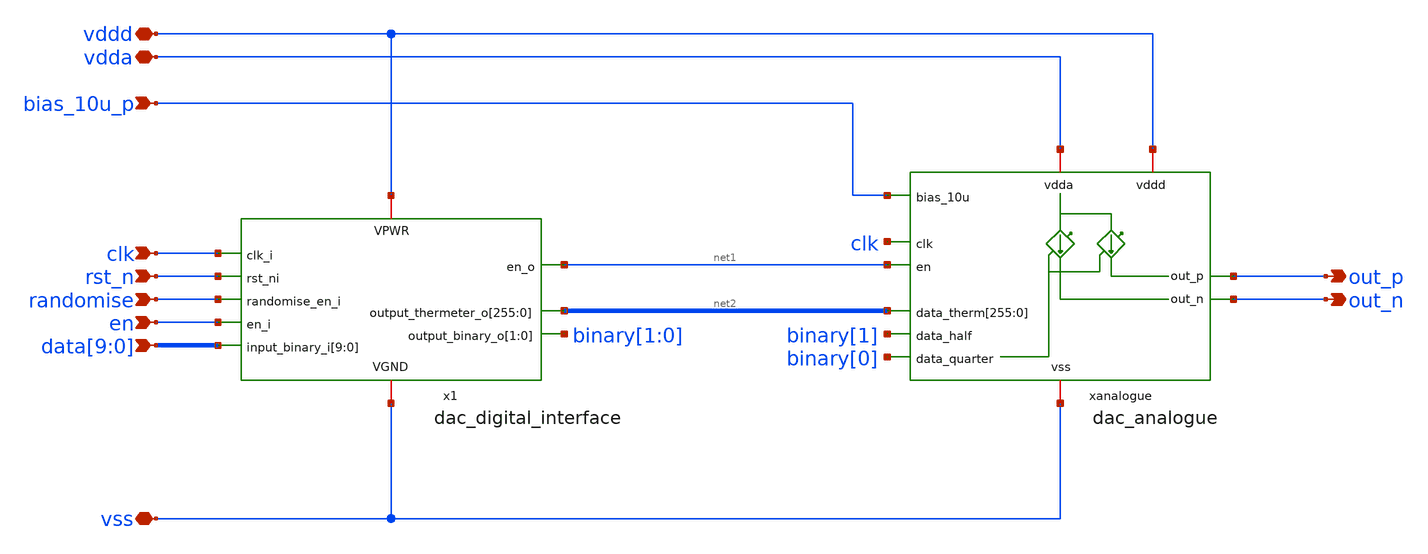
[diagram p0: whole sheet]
** sch_path: design/dac/dac.sch
**.subckt dac vss vdda vddd bias_10u_p clk
*+ data[9],data[8],data[7],data[6],data[5],data[4],data[3],data[2],data[1],data[0] out_p out_n en randomise rst_n
*.iopin vss
*.iopin vdda
*.iopin vddd
*.ipin bias_10u_p
*.ipin clk
*.ipin data[9],data[8],data[7],data[6],data[5],data[4],data[3],data[2],data[1],data[0]
*.opin out_p
*.opin out_n
*.ipin en
*.ipin randomise
*.ipin rst_n
xanalogue vdda vddd bias_10u_p clk net1 net2[255] net2[254] net2[253] net2[252] net2[251] net2[250]
+ net2[249] net2[248] net2[247] net2[246] net2[245] net2[244] net2[243] net2[242] net2[241] net2[240] net2[239]
+ net2[238] net2[237] net2[236] net2[235] net2[234] net2[233] net2[232] net2[231] net2[230] net2[229] net2[228]
+ net2[227] net2[226] net2[225] net2[224] net2[223] net2[222] net2[221] net2[220] net2[219] net2[218] net2[217]
+ net2[216] net2[215] net2[214] net2[213] net2[212] net2[211] net2[210] net2[209] net2[208] net2[207] net2[206]
+ net2[205] net2[204] net2[203] net2[202] net2[201] net2[200] net2[199] net2[198] net2[197] net2[196] net2[195]
+ net2[194] net2[193] net2[192] net2[191] net2[190] net2[189] net2[188] net2[187] net2[186] net2[185] net2[184]
+ net2[183] net2[182] net2[181] net2[180] net2[179] net2[178] net2[177] net2[176] net2[175] net2[174] net2[173]
+ net2[172] net2[171] net2[170] net2[169] net2[168] net2[167] net2[166] net2[165] net2[164] net2[163] net2[162]
+ net2[161] net2[160] net2[159] net2[158] net2[157] net2[156] net2[155] net2[154] net2[153] net2[152] net2[151]
+ net2[150] net2[149] net2[148] net2[147] net2[146] net2[145] net2[144] net2[143] net2[142] net2[141] net2[140]
+ net2[139] net2[138] net2[137] net2[136] net2[135] net2[134] net2[133] net2[132] net2[131] net2[130] net2[129]
+ net2[128] net2[127] net2[126] net2[125] net2[124] net2[123] net2[122] net2[121] net2[120] net2[119] net2[118]
+ net2[117] net2[116] net2[115] net2[114] net2[113] net2[112] net2[111] net2[110] net2[109] net2[108] net2[107]
+ net2[106] net2[105] net2[104] net2[103] net2[102] net2[101] net2[100] net2[99] net2[98] net2[97] net2[96]
+ net2[95] net2[94] net2[93] net2[92] net2[91] net2[90] net2[89] net2[88] net2[87] net2[86] net2[85] net2[84]
+ net2[83] net2[82] net2[81] net2[80] net2[79] net2[78] net2[77] net2[76] net2[75] net2[74] net2[73] net2[72]
+ net2[71] net2[70] net2[69] net2[68] net2[67] net2[66] net2[65] net2[64] net2[63] net2[62] net2[61] net2[60]
+ net2[59] net2[58] net2[57] net2[56] net2[55] net2[54] net2[53] net2[52] net2[51] net2[50] net2[49] net2[48]
+ net2[47] net2[46] net2[45] net2[44] net2[43] net2[42] net2[41] net2[40] net2[39] net2[38] net2[37] net2[36]
+ net2[35] net2[34] net2[33] net2[32] net2[31] net2[30] net2[29] net2[28] net2[27] net2[26] net2[25] net2[24]
+ net2[23] net2[22] net2[21] net2[20] net2[19] net2[18] net2[17] net2[16] net2[15] net2[14] net2[13] net2[12]
+ net2[11] net2[10] net2[9] net2[8] net2[7] net2[6] net2[5] net2[4] net2[3] net2[2] net2[1] net2[0] binary[1]
+ binary[0] out_p out_n vss dac_analogue
x1 vddd clk net2[255] net2[254] net2[253] net2[252] net2[251] net2[250] net2[249] net2[248]
+ net2[247] net2[246] net2[245] net2[244] net2[243] net2[242] net2[241] net2[240] net2[239] net2[238] net2[237]
+ net2[236] net2[235] net2[234] net2[233] net2[232] net2[231] net2[230] net2[229] net2[228] net2[227] net2[226]
+ net2[225] net2[224] net2[223] net2[222] net2[221] net2[220] net2[219] net2[218] net2[217] net2[216] net2[215]
+ net2[214] net2[213] net2[212] net2[211] net2[210] net2[209] net2[208] net2[207] net2[206] net2[205] net2[204]
+ net2[203] net2[202] net2[201] net2[200] net2[199] net2[198] net2[197] net2[196] net2[195] net2[194] net2[193]
+ net2[192] net2[191] net2[190] net2[189] net2[188] net2[187] net2[186] net2[185] net2[184] net2[183] net2[182]
+ net2[181] net2[180] net2[179] net2[178] net2[177] net2[176] net2[175] net2[174] net2[173] net2[172] net2[171]
+ net2[170] net2[169] net2[168] net2[167] net2[166] net2[165] net2[164] net2[163] net2[162] net2[161] net2[160]
+ net2[159] net2[158] net2[157] net2[156] net2[155] net2[154] net2[153] net2[152] net2[151] net2[150] net2[149]
+ net2[148] net2[147] net2[146] net2[145] net2[144] net2[143] net2[142] net2[141] net2[140] net2[139] net2[138]
+ net2[137] net2[136] net2[135] net2[134] net2[133] net2[132] net2[131] net2[130] net2[129] net2[128] net2[127]
+ net2[126] net2[125] net2[124] net2[123] net2[122] net2[121] net2[120] net2[119] net2[118] net2[117] net2[116]
+ net2[115] net2[114] net2[113] net2[112] net2[111] net2[110] net2[109] net2[108] net2[107] net2[106] net2[105]
+ net2[104] net2[103] net2[102] net2[101] net2[100] net2[99] net2[98] net2[97] net2[96] net2[95] net2[94]
+ net2[93] net2[92] net2[91] net2[90] net2[89] net2[88] net2[87] net2[86] net2[85] net2[84] net2[83] net2[82]
+ net2[81] net2[80] net2[79] net2[78] net2[77] net2[76] net2[75] net2[74] net2[73] net2[72] net2[71] net2[70]
+ net2[69] net2[68] net2[67] net2[66] net2[65] net2[64] net2[63] net2[62] net2[61] net2[60] net2[59] net2[58]
+ net2[57] net2[56] net2[55] net2[54] net2[53] net2[52] net2[51] net2[50] net2[49] net2[48] net2[47] net2[46]
+ net2[45] net2[44] net2[43] net2[42] net2[41] net2[40] net2[39] net2[38] net2[37] net2[36] net2[35] net2[34]
+ net2[33] net2[32] net2[31] net2[30] net2[29] net2[28] net2[27] net2[26] net2[25] net2[24] net2[23] net2[22]
+ net2[21] net2[20] net2[19] net2[18] net2[17] net2[16] net2[15] net2[14] net2[13] net2[12] net2[11] net2[10]
+ net2[9] net2[8] net2[7] net2[6] net2[5] net2[4] net2[3] net2[2] net2[1] net2[0] rst_n binary[1] binary[0]
+ randomise net1 en data[9] data[8] data[7] data[6] data[5] data[4] data[3] data[2] data[1] data[0] vss
+ dac_digital_interface
**.ends
.end
